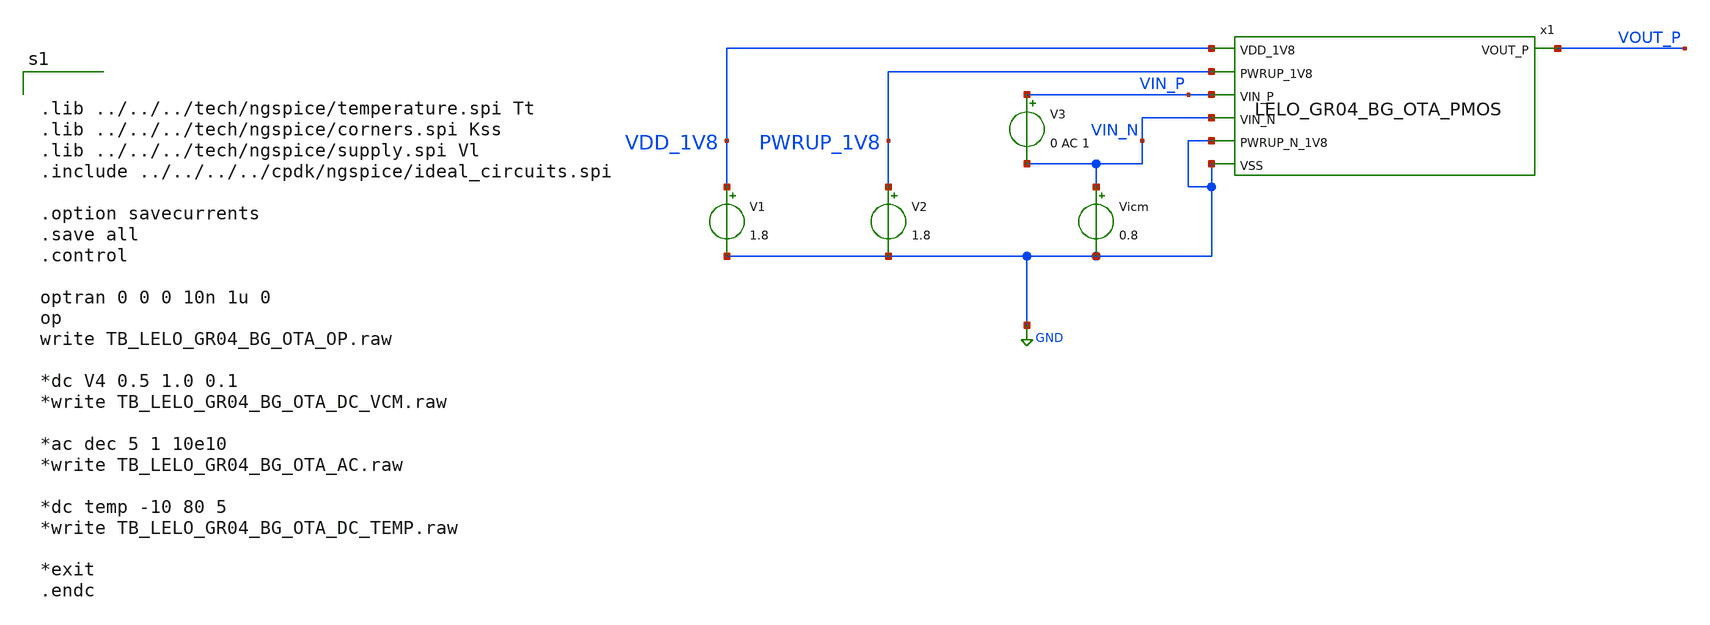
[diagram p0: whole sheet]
** sch_path: design/LELO_GR04_SKY130A/TB_LELO_GR04_BG_OTA.sch
**.subckt TB_LELO_GR04_BG_OTA
V1 VDD_1V8 GND 1.8
V2 PWRUP_1V8 GND 1.8
Vicm VIN_N GND 0.8
x1 VDD_1V8 PWRUP_1V8 VIN_P VIN_N GND VOUT_P GND LELO_GR04_BG_OTA_PMOS
V3 VIN_P VIN_N 0 AC 1
**** begin user architecture code


.lib ../../../tech/ngspice/temperature.spi Tt
.lib ../../../tech/ngspice/corners.spi Kss
.lib ../../../tech/ngspice/supply.spi Vl
.include ../../../../cpdk/ngspice/ideal_circuits.spi

.option savecurrents
.save all
.control

optran 0 0 0 10n 1u 0
op
write TB_LELO_GR04_BG_OTA_OP.raw

*dc V4 0.5 1.0 0.1
*write TB_LELO_GR04_BG_OTA_DC_VCM.raw

*ac dec 5 1 10e10
*write TB_LELO_GR04_BG_OTA_AC.raw

*dc temp -10 80 5
*write TB_LELO_GR04_BG_OTA_DC_TEMP.raw

*exit
.endc


**** end user architecture code
**.ends
.GLOBAL GND
.end
